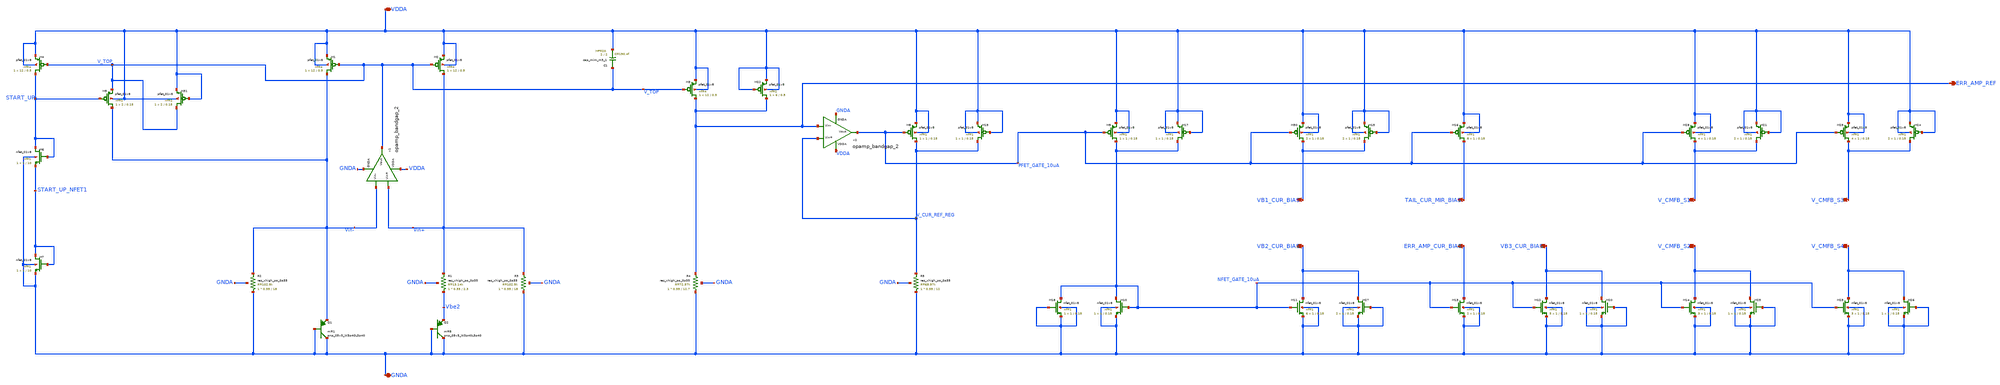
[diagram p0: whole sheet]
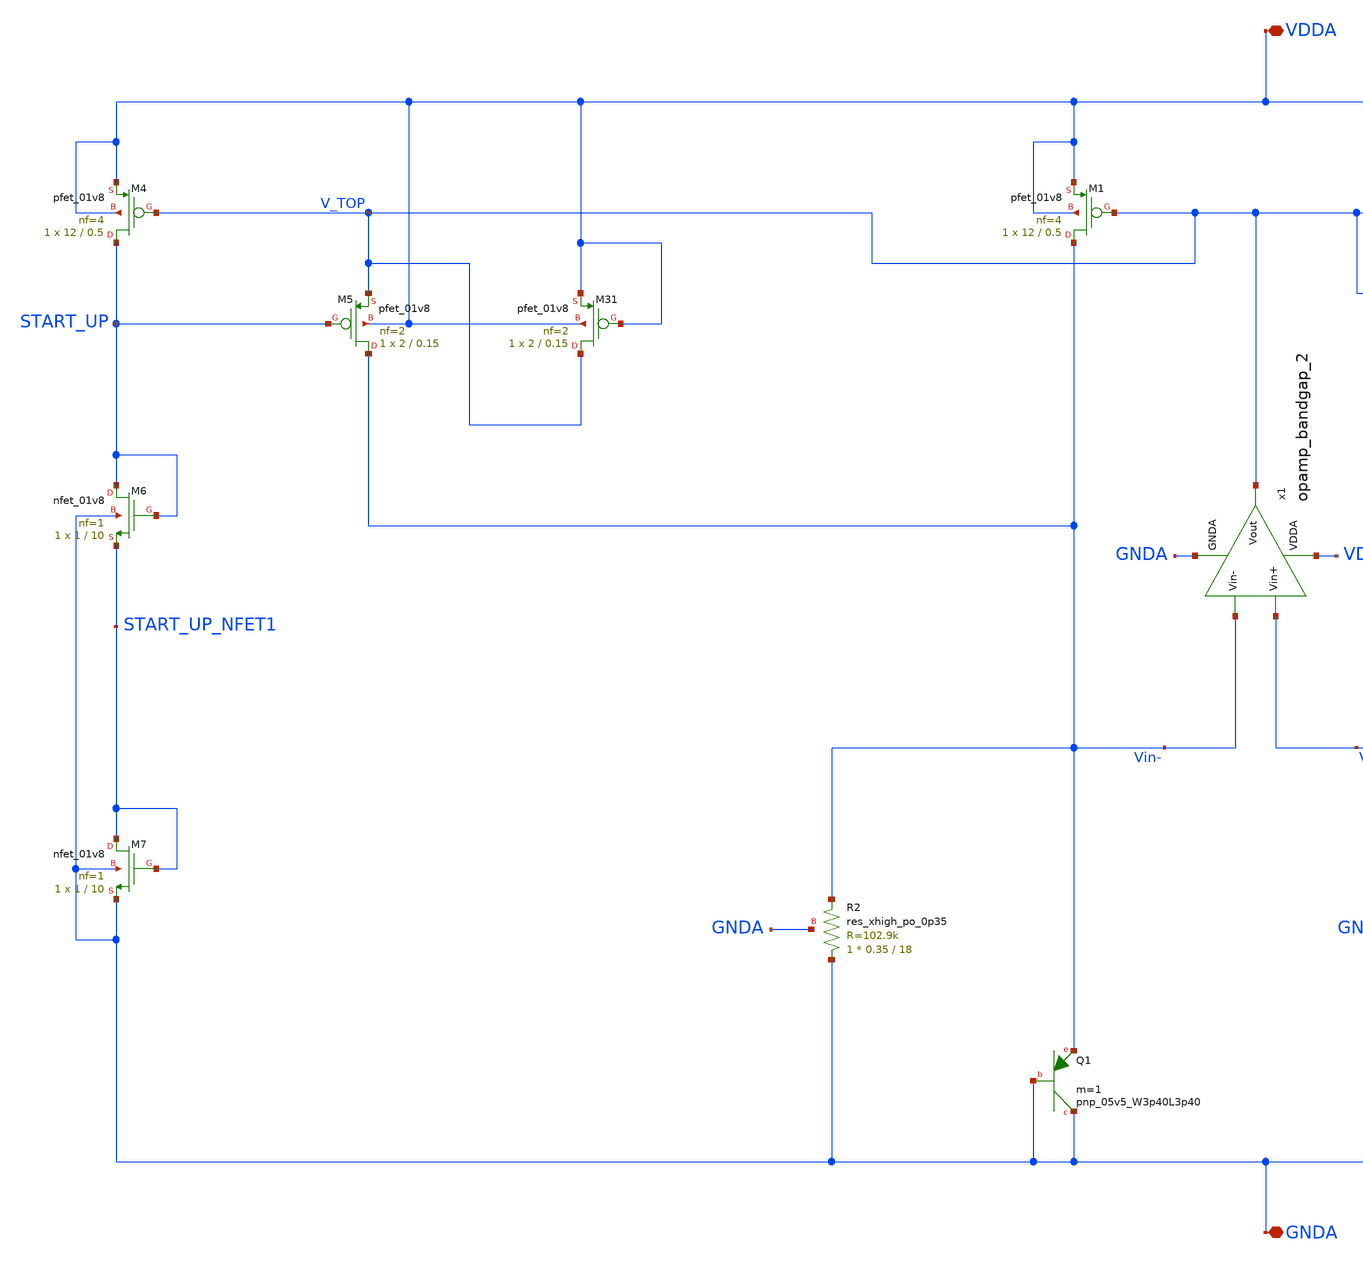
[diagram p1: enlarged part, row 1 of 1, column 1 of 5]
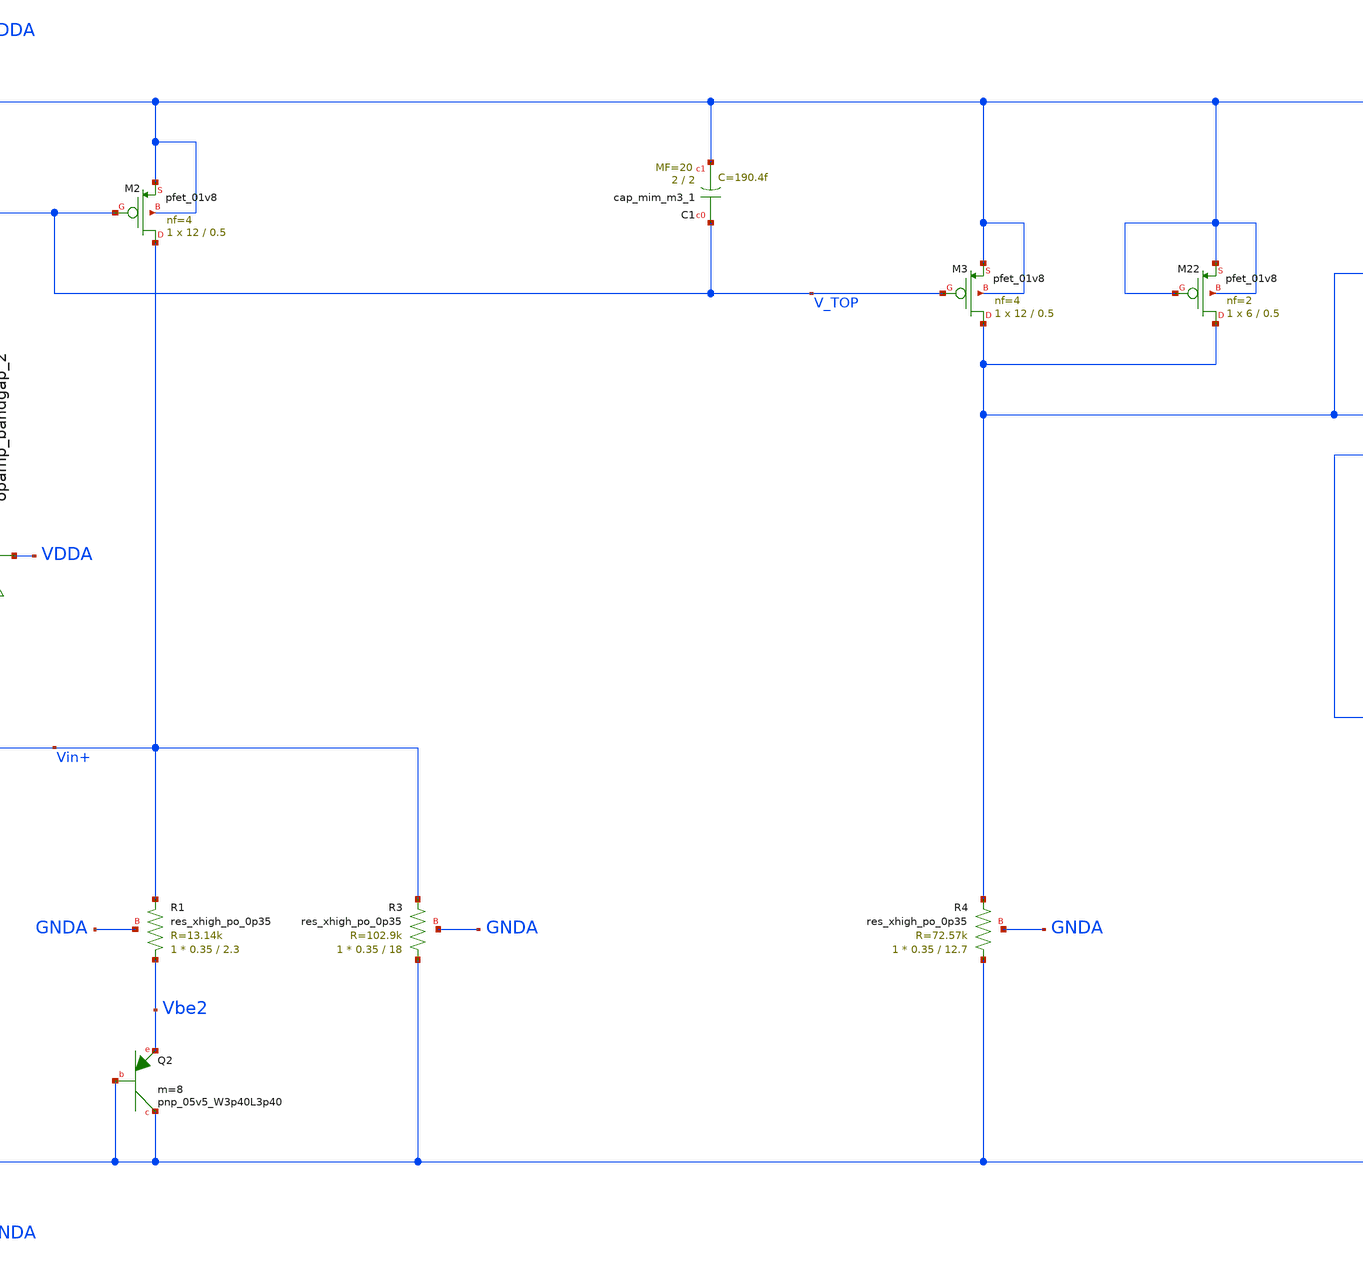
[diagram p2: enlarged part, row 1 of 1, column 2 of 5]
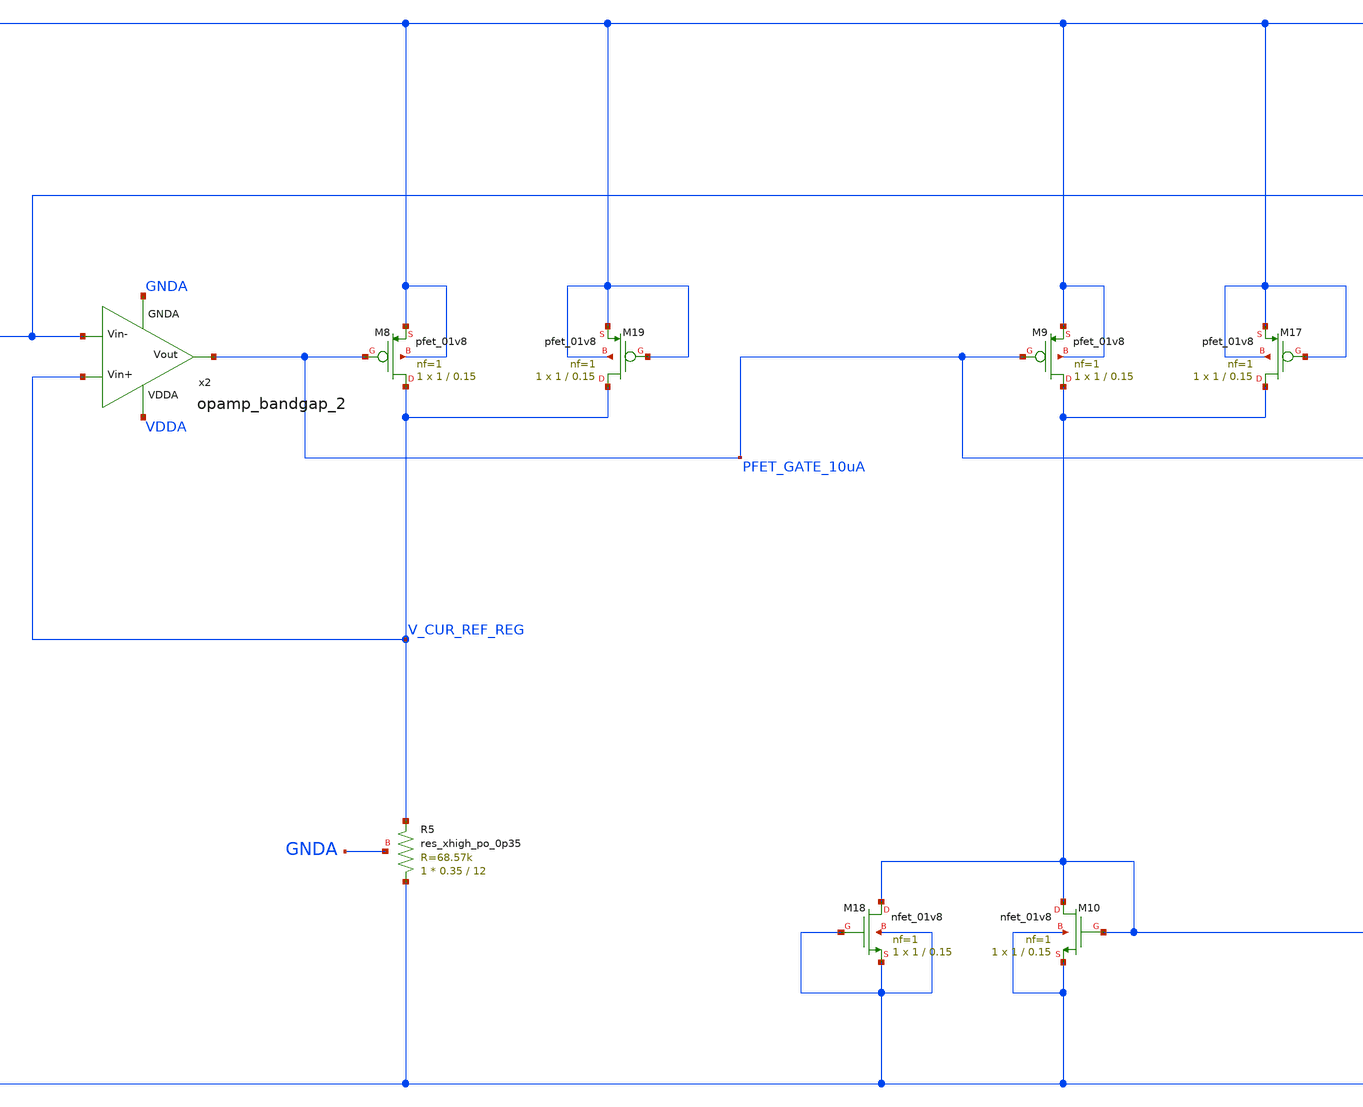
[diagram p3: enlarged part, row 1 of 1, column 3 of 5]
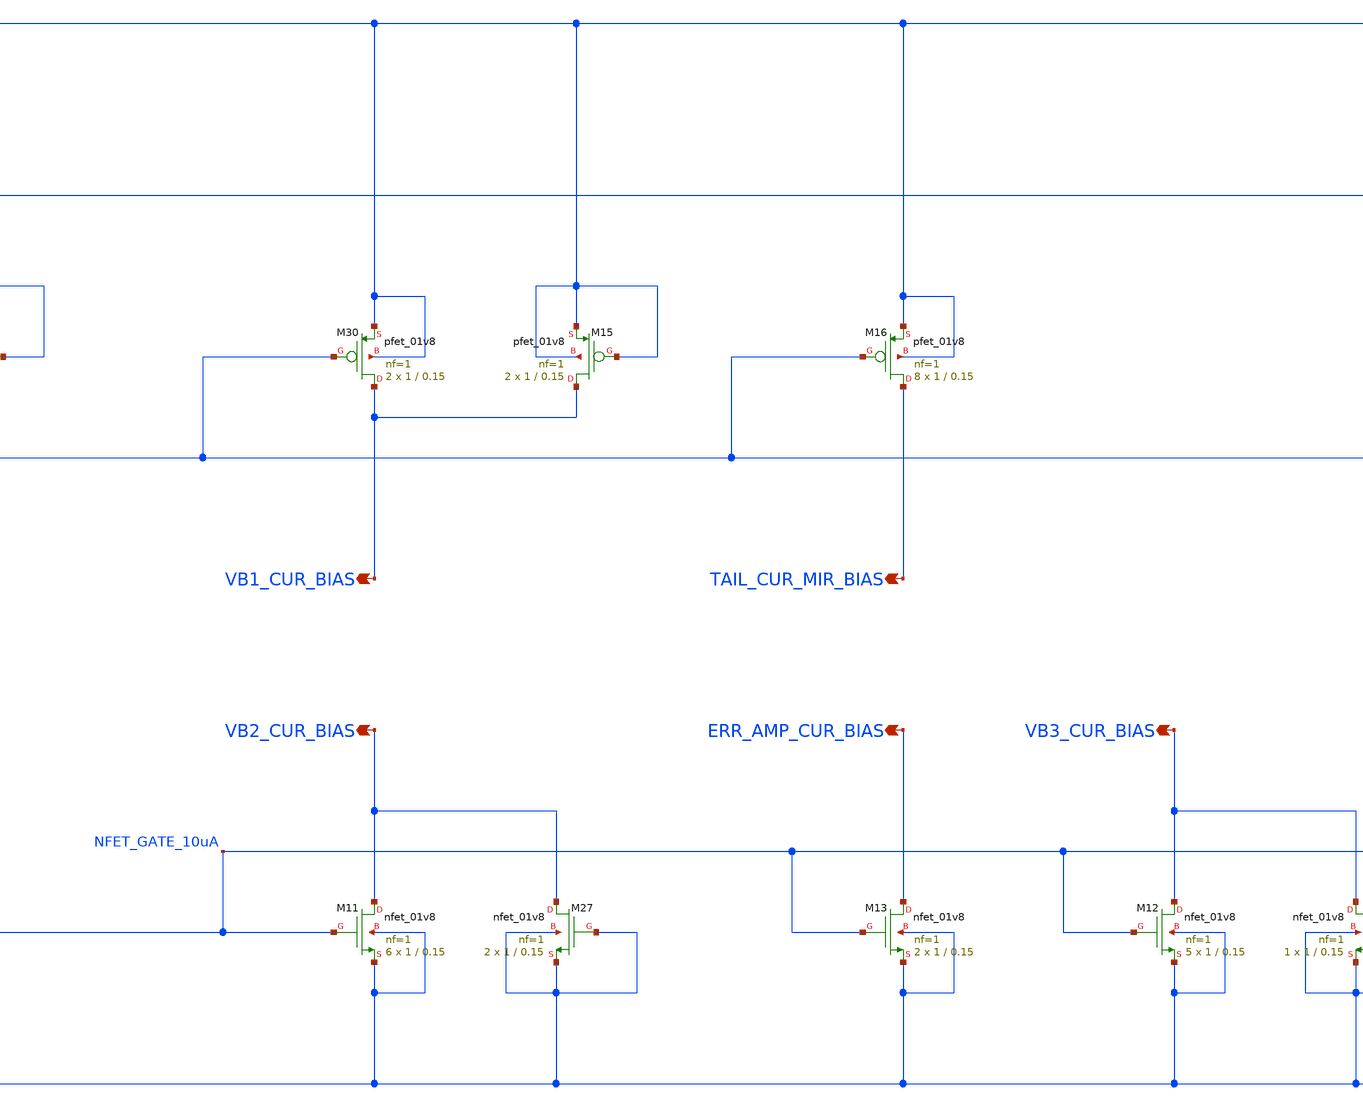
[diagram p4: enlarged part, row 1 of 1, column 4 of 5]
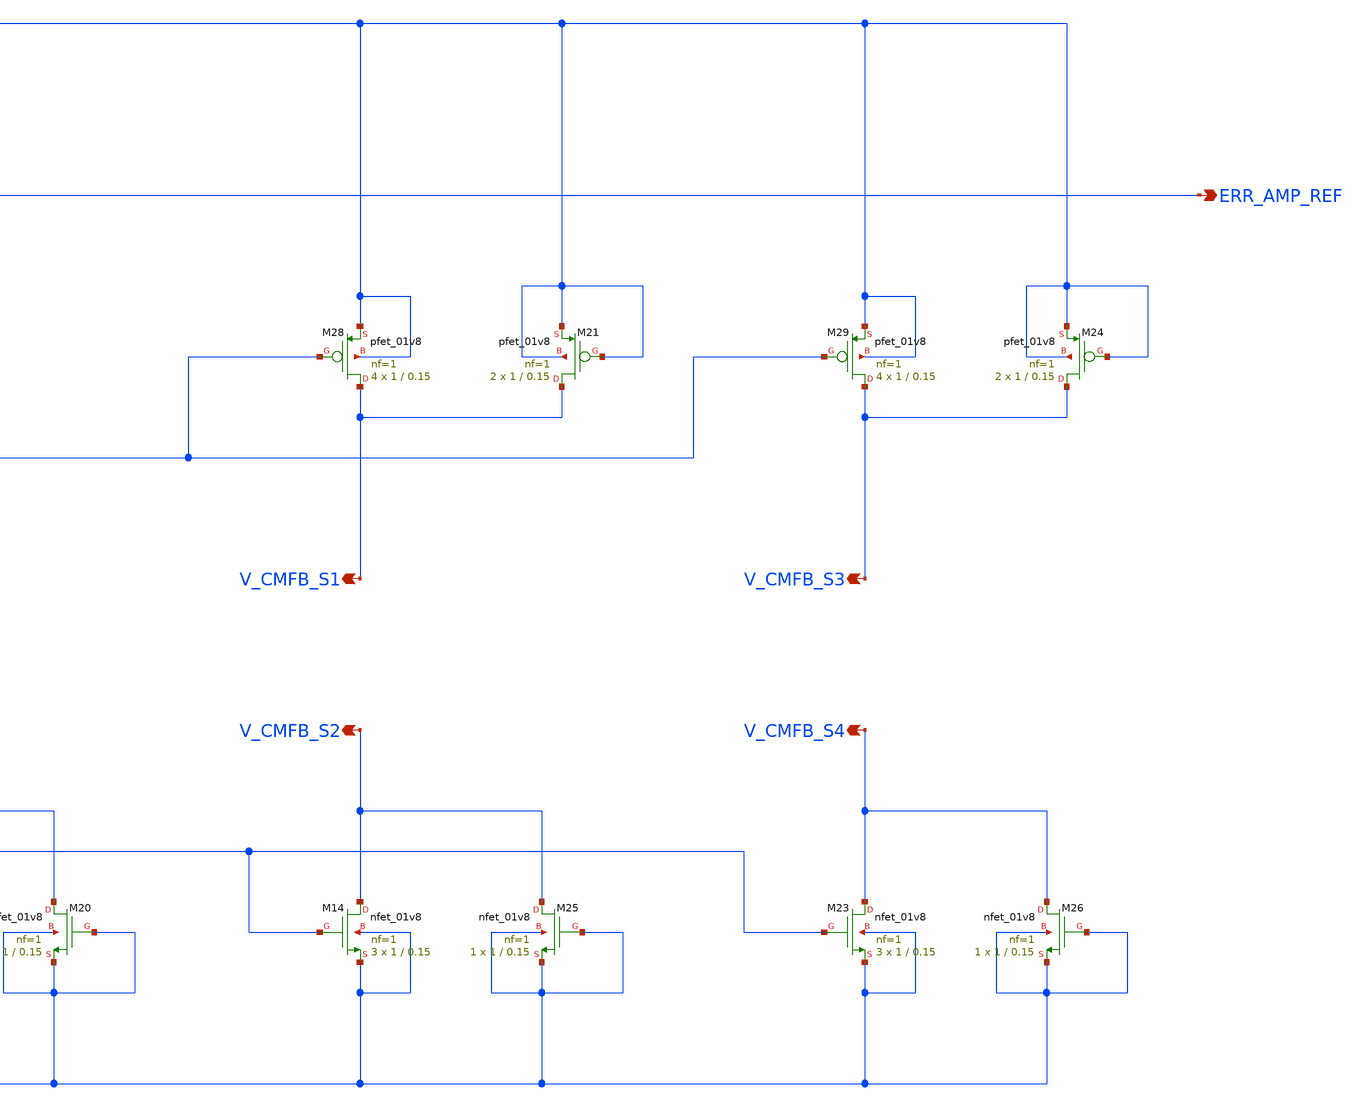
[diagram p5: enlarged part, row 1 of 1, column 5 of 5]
** sch_path: projects/opamp/xschem_ngspice/ref_volt_cur_gen_dummy.sch
**.subckt ref_volt_cur_gen_dummy VB1_CUR_BIAS GNDA ERR_AMP_REF VDDA VB2_CUR_BIAS VB3_CUR_BIAS
*+ ERR_AMP_CUR_BIAS V_CMFB_S2 TAIL_CUR_MIR_BIAS V_CMFB_S1 V_CMFB_S4 V_CMFB_S3
*.opin VB1_CUR_BIAS
*.iopin GNDA
*.opin ERR_AMP_REF
*.iopin VDDA
*.opin VB2_CUR_BIAS
*.opin VB3_CUR_BIAS
*.opin ERR_AMP_CUR_BIAS
*.opin V_CMFB_S2
*.opin TAIL_CUR_MIR_BIAS
*.opin V_CMFB_S1
*.opin V_CMFB_S4
*.opin V_CMFB_S3
XM3 ERR_AMP_REF V_TOP VDDA VDDA sky130_fd_pr__pfet_01v8 L=0.5 W=12 nf=4 ad='int((nf+1)/2) * W/nf * 0.29'
+ as='int((nf+2)/2) * W/nf * 0.29' pd='2*int((nf+1)/2) * (W/nf + 0.29)' ps='2*int((nf+2)/2) * (W/nf + 0.29)'
+ nrd='0.29 / W' nrs='0.29 / W' sa=0 sb=0 sd=0 mult=1 m=1
XR4 GNDA ERR_AMP_REF GNDA sky130_fd_pr__res_xhigh_po_0p35 L=12.7 mult=1 m=1
XR5 GNDA V_CUR_REF_REG GNDA sky130_fd_pr__res_xhigh_po_0p35 L=12 mult=1 m=1
XM8 V_CUR_REF_REG PFET_GATE_10uA VDDA VDDA sky130_fd_pr__pfet_01v8 L=0.15 W=1 nf=1 ad='int((nf+1)/2) * W/nf * 0.29'
+ as='int((nf+2)/2) * W/nf * 0.29' pd='2*int((nf+1)/2) * (W/nf + 0.29)' ps='2*int((nf+2)/2) * (W/nf + 0.29)'
+ nrd='0.29 / W' nrs='0.29 / W' sa=0 sb=0 sd=0 mult=1 m=1
XC1 V_TOP VDDA sky130_fd_pr__cap_mim_m3_1 W=2 L=2 MF=20 m=20
XQ1 GNDA GNDA Vin- sky130_fd_pr__pnp_05v5_W3p40L3p40 m=1
XQ2 GNDA GNDA Vbe2 sky130_fd_pr__pnp_05v5_W3p40L3p40 m=8
XM1 Vin- V_TOP VDDA VDDA sky130_fd_pr__pfet_01v8 L=0.5 W=12 nf=4 ad='int((nf+1)/2) * W/nf * 0.29' as='int((nf+2)/2) * W/nf * 0.29'
+ pd='2*int((nf+1)/2) * (W/nf + 0.29)' ps='2*int((nf+2)/2) * (W/nf + 0.29)' nrd='0.29 / W' nrs='0.29 / W'
+ sa=0 sb=0 sd=0 mult=1 m=1
XM2 Vin+ V_TOP VDDA VDDA sky130_fd_pr__pfet_01v8 L=0.5 W=12 nf=4 ad='int((nf+1)/2) * W/nf * 0.29' as='int((nf+2)/2) * W/nf * 0.29'
+ pd='2*int((nf+1)/2) * (W/nf + 0.29)' ps='2*int((nf+2)/2) * (W/nf + 0.29)' nrd='0.29 / W' nrs='0.29 / W'
+ sa=0 sb=0 sd=0 mult=1 m=1
XR1 Vbe2 Vin+ GNDA sky130_fd_pr__res_xhigh_po_0p35 L=2.3 mult=1 m=1
XR3 GNDA Vin+ GNDA sky130_fd_pr__res_xhigh_po_0p35 L=18 mult=1 m=1
XR2 GNDA Vin- GNDA sky130_fd_pr__res_xhigh_po_0p35 L=18 mult=1 m=1
XM6 START_UP START_UP START_UP_NFET1 GNDA sky130_fd_pr__nfet_01v8 L=10 W=1 nf=1 ad='int((nf+1)/2) * W/nf * 0.29'
+ as='int((nf+2)/2) * W/nf * 0.29' pd='2*int((nf+1)/2) * (W/nf + 0.29)' ps='2*int((nf+2)/2) * (W/nf + 0.29)'
+ nrd='0.29 / W' nrs='0.29 / W' sa=0 sb=0 sd=0 mult=1 m=1
XM4 START_UP V_TOP VDDA VDDA sky130_fd_pr__pfet_01v8 L=0.5 W=12 nf=4 ad='int((nf+1)/2) * W/nf * 0.29'
+ as='int((nf+2)/2) * W/nf * 0.29' pd='2*int((nf+1)/2) * (W/nf + 0.29)' ps='2*int((nf+2)/2) * (W/nf + 0.29)'
+ nrd='0.29 / W' nrs='0.29 / W' sa=0 sb=0 sd=0 mult=1 m=1
XM5 Vin- START_UP V_TOP VDDA sky130_fd_pr__pfet_01v8 L=0.15 W=2 nf=2 ad='int((nf+1)/2) * W/nf * 0.29'
+ as='int((nf+2)/2) * W/nf * 0.29' pd='2*int((nf+1)/2) * (W/nf + 0.29)' ps='2*int((nf+2)/2) * (W/nf + 0.29)'
+ nrd='0.29 / W' nrs='0.29 / W' sa=0 sb=0 sd=0 mult=1 m=1
XM7 START_UP_NFET1 START_UP_NFET1 GNDA GNDA sky130_fd_pr__nfet_01v8 L=10 W=1 nf=1 ad='int((nf+1)/2) * W/nf * 0.29'
+ as='int((nf+2)/2) * W/nf * 0.29' pd='2*int((nf+1)/2) * (W/nf + 0.29)' ps='2*int((nf+2)/2) * (W/nf + 0.29)'
+ nrd='0.29 / W' nrs='0.29 / W' sa=0 sb=0 sd=0 mult=1 m=1
x1 VDDA V_TOP Vin- Vin+ GNDA opamp_bandgap_2
x2 VDDA PFET_GATE_10uA ERR_AMP_REF V_CUR_REF_REG GNDA opamp_bandgap_2
XM9 NFET_GATE_10uA PFET_GATE_10uA VDDA VDDA sky130_fd_pr__pfet_01v8 L=0.15 W=1 nf=1 ad='int((nf+1)/2) * W/nf * 0.29'
+ as='int((nf+2)/2) * W/nf * 0.29' pd='2*int((nf+1)/2) * (W/nf + 0.29)' ps='2*int((nf+2)/2) * (W/nf + 0.29)'
+ nrd='0.29 / W' nrs='0.29 / W' sa=0 sb=0 sd=0 mult=1 m=1
XM10 NFET_GATE_10uA NFET_GATE_10uA GNDA GNDA sky130_fd_pr__nfet_01v8 L=0.15 W=1 nf=1 ad='int((nf+1)/2) * W/nf * 0.29'
+ as='int((nf+2)/2) * W/nf * 0.29' pd='2*int((nf+1)/2) * (W/nf + 0.29)' ps='2*int((nf+2)/2) * (W/nf + 0.29)'
+ nrd='0.29 / W' nrs='0.29 / W' sa=0 sb=0 sd=0 mult=1 m=1
XM11 VB2_CUR_BIAS NFET_GATE_10uA GNDA GNDA sky130_fd_pr__nfet_01v8 L=0.15 W=1 nf=1 ad='int((nf+1)/2) * W/nf * 0.29'
+ as='int((nf+2)/2) * W/nf * 0.29' pd='2*int((nf+1)/2) * (W/nf + 0.29)' ps='2*int((nf+2)/2) * (W/nf + 0.29)'
+ nrd='0.29 / W' nrs='0.29 / W' sa=0 sb=0 sd=0 mult=6 m=6
XM12 VB3_CUR_BIAS NFET_GATE_10uA GNDA GNDA sky130_fd_pr__nfet_01v8 L=0.15 W=1 nf=1 ad='int((nf+1)/2) * W/nf * 0.29'
+ as='int((nf+2)/2) * W/nf * 0.29' pd='2*int((nf+1)/2) * (W/nf + 0.29)' ps='2*int((nf+2)/2) * (W/nf + 0.29)'
+ nrd='0.29 / W' nrs='0.29 / W' sa=0 sb=0 sd=0 mult=5 m=5
XM30 VB1_CUR_BIAS PFET_GATE_10uA VDDA VDDA sky130_fd_pr__pfet_01v8 L=0.15 W=1 nf=1 ad='int((nf+1)/2) * W/nf * 0.29'
+ as='int((nf+2)/2) * W/nf * 0.29' pd='2*int((nf+1)/2) * (W/nf + 0.29)' ps='2*int((nf+2)/2) * (W/nf + 0.29)'
+ nrd='0.29 / W' nrs='0.29 / W' sa=0 sb=0 sd=0 mult=2 m=2
XM13 ERR_AMP_CUR_BIAS NFET_GATE_10uA GNDA GNDA sky130_fd_pr__nfet_01v8 L=0.15 W=1 nf=1 ad='int((nf+1)/2) * W/nf * 0.29'
+ as='int((nf+2)/2) * W/nf * 0.29' pd='2*int((nf+1)/2) * (W/nf + 0.29)' ps='2*int((nf+2)/2) * (W/nf + 0.29)'
+ nrd='0.29 / W' nrs='0.29 / W' sa=0 sb=0 sd=0 mult=2 m=2
XM14 V_CMFB_S2 NFET_GATE_10uA GNDA GNDA sky130_fd_pr__nfet_01v8 L=0.15 W=1 nf=1 ad='int((nf+1)/2) * W/nf * 0.29'
+ as='int((nf+2)/2) * W/nf * 0.29' pd='2*int((nf+1)/2) * (W/nf + 0.29)' ps='2*int((nf+2)/2) * (W/nf + 0.29)'
+ nrd='0.29 / W' nrs='0.29 / W' sa=0 sb=0 sd=0 mult=3 m=3
XM16 TAIL_CUR_MIR_BIAS PFET_GATE_10uA VDDA VDDA sky130_fd_pr__pfet_01v8 L=0.15 W=1 nf=1 ad='int((nf+1)/2) * W/nf * 0.29'
+ as='int((nf+2)/2) * W/nf * 0.29' pd='2*int((nf+1)/2) * (W/nf + 0.29)' ps='2*int((nf+2)/2) * (W/nf + 0.29)'
+ nrd='0.29 / W' nrs='0.29 / W' sa=0 sb=0 sd=0 mult=8 m=8
XM17 NFET_GATE_10uA VDDA VDDA VDDA sky130_fd_pr__pfet_01v8 L=0.15 W=1 nf=1 ad='int((nf+1)/2) * W/nf * 0.29'
+ as='int((nf+2)/2) * W/nf * 0.29' pd='2*int((nf+1)/2) * (W/nf + 0.29)' ps='2*int((nf+2)/2) * (W/nf + 0.29)'
+ nrd='0.29 / W' nrs='0.29 / W' sa=0 sb=0 sd=0 mult=1 m=1
XM18 NFET_GATE_10uA GNDA GNDA GNDA sky130_fd_pr__nfet_01v8 L=0.15 W=1 nf=1 ad='int((nf+1)/2) * W/nf * 0.29'
+ as='int((nf+2)/2) * W/nf * 0.29' pd='2*int((nf+1)/2) * (W/nf + 0.29)' ps='2*int((nf+2)/2) * (W/nf + 0.29)'
+ nrd='0.29 / W' nrs='0.29 / W' sa=0 sb=0 sd=0 mult=1 m=1
XM19 V_CUR_REF_REG VDDA VDDA VDDA sky130_fd_pr__pfet_01v8 L=0.15 W=1 nf=1 ad='int((nf+1)/2) * W/nf * 0.29'
+ as='int((nf+2)/2) * W/nf * 0.29' pd='2*int((nf+1)/2) * (W/nf + 0.29)' ps='2*int((nf+2)/2) * (W/nf + 0.29)'
+ nrd='0.29 / W' nrs='0.29 / W' sa=0 sb=0 sd=0 mult=1 m=1
XM20 VB3_CUR_BIAS GNDA GNDA GNDA sky130_fd_pr__nfet_01v8 L=0.15 W=1 nf=1 ad='int((nf+1)/2) * W/nf * 0.29'
+ as='int((nf+2)/2) * W/nf * 0.29' pd='2*int((nf+1)/2) * (W/nf + 0.29)' ps='2*int((nf+2)/2) * (W/nf + 0.29)'
+ nrd='0.29 / W' nrs='0.29 / W' sa=0 sb=0 sd=0 mult=1 m=1
XM28 V_CMFB_S1 PFET_GATE_10uA VDDA VDDA sky130_fd_pr__pfet_01v8 L=0.15 W=1 nf=1 ad='int((nf+1)/2) * W/nf * 0.29'
+ as='int((nf+2)/2) * W/nf * 0.29' pd='2*int((nf+1)/2) * (W/nf + 0.29)' ps='2*int((nf+2)/2) * (W/nf + 0.29)'
+ nrd='0.29 / W' nrs='0.29 / W' sa=0 sb=0 sd=0 mult=4 m=4
XM22 ERR_AMP_REF VDDA VDDA VDDA sky130_fd_pr__pfet_01v8 L=0.5 W=6 nf=2 ad='int((nf+1)/2) * W/nf * 0.29'
+ as='int((nf+2)/2) * W/nf * 0.29' pd='2*int((nf+1)/2) * (W/nf + 0.29)' ps='2*int((nf+2)/2) * (W/nf + 0.29)'
+ nrd='0.29 / W' nrs='0.29 / W' sa=0 sb=0 sd=0 mult=1 m=1
XM23 V_CMFB_S4 NFET_GATE_10uA GNDA GNDA sky130_fd_pr__nfet_01v8 L=0.15 W=1 nf=1 ad='int((nf+1)/2) * W/nf * 0.29'
+ as='int((nf+2)/2) * W/nf * 0.29' pd='2*int((nf+1)/2) * (W/nf + 0.29)' ps='2*int((nf+2)/2) * (W/nf + 0.29)'
+ nrd='0.29 / W' nrs='0.29 / W' sa=0 sb=0 sd=0 mult=3 m=3
XM29 V_CMFB_S3 PFET_GATE_10uA VDDA VDDA sky130_fd_pr__pfet_01v8 L=0.15 W=1 nf=1 ad='int((nf+1)/2) * W/nf * 0.29'
+ as='int((nf+2)/2) * W/nf * 0.29' pd='2*int((nf+1)/2) * (W/nf + 0.29)' ps='2*int((nf+2)/2) * (W/nf + 0.29)'
+ nrd='0.29 / W' nrs='0.29 / W' sa=0 sb=0 sd=0 mult=4 m=4
XM25 V_CMFB_S2 GNDA GNDA GNDA sky130_fd_pr__nfet_01v8 L=0.15 W=1 nf=1 ad='int((nf+1)/2) * W/nf * 0.29'
+ as='int((nf+2)/2) * W/nf * 0.29' pd='2*int((nf+1)/2) * (W/nf + 0.29)' ps='2*int((nf+2)/2) * (W/nf + 0.29)'
+ nrd='0.29 / W' nrs='0.29 / W' sa=0 sb=0 sd=0 mult=1 m=1
XM26 V_CMFB_S4 GNDA GNDA GNDA sky130_fd_pr__nfet_01v8 L=0.15 W=1 nf=1 ad='int((nf+1)/2) * W/nf * 0.29'
+ as='int((nf+2)/2) * W/nf * 0.29' pd='2*int((nf+1)/2) * (W/nf + 0.29)' ps='2*int((nf+2)/2) * (W/nf + 0.29)'
+ nrd='0.29 / W' nrs='0.29 / W' sa=0 sb=0 sd=0 mult=1 m=1
XM27 VB2_CUR_BIAS GNDA GNDA GNDA sky130_fd_pr__nfet_01v8 L=0.15 W=1 nf=1 ad='int((nf+1)/2) * W/nf * 0.29'
+ as='int((nf+2)/2) * W/nf * 0.29' pd='2*int((nf+1)/2) * (W/nf + 0.29)' ps='2*int((nf+2)/2) * (W/nf + 0.29)'
+ nrd='0.29 / W' nrs='0.29 / W' sa=0 sb=0 sd=0 mult=2 m=2
XM21 V_CMFB_S1 VDDA VDDA VDDA sky130_fd_pr__pfet_01v8 L=0.15 W=1 nf=1 ad='int((nf+1)/2) * W/nf * 0.29'
+ as='int((nf+2)/2) * W/nf * 0.29' pd='2*int((nf+1)/2) * (W/nf + 0.29)' ps='2*int((nf+2)/2) * (W/nf + 0.29)'
+ nrd='0.29 / W' nrs='0.29 / W' sa=0 sb=0 sd=0 mult=2 m=2
XM24 V_CMFB_S3 VDDA VDDA VDDA sky130_fd_pr__pfet_01v8 L=0.15 W=1 nf=1 ad='int((nf+1)/2) * W/nf * 0.29'
+ as='int((nf+2)/2) * W/nf * 0.29' pd='2*int((nf+1)/2) * (W/nf + 0.29)' ps='2*int((nf+2)/2) * (W/nf + 0.29)'
+ nrd='0.29 / W' nrs='0.29 / W' sa=0 sb=0 sd=0 mult=2 m=2
XM15 VB1_CUR_BIAS VDDA VDDA VDDA sky130_fd_pr__pfet_01v8 L=0.15 W=1 nf=1 ad='int((nf+1)/2) * W/nf * 0.29'
+ as='int((nf+2)/2) * W/nf * 0.29' pd='2*int((nf+1)/2) * (W/nf + 0.29)' ps='2*int((nf+2)/2) * (W/nf + 0.29)'
+ nrd='0.29 / W' nrs='0.29 / W' sa=0 sb=0 sd=0 mult=2 m=2
XM31 V_TOP VDDA VDDA VDDA sky130_fd_pr__pfet_01v8 L=0.15 W=2 nf=2 ad='int((nf+1)/2) * W/nf * 0.29' as='int((nf+2)/2) * W/nf * 0.29'
+ pd='2*int((nf+1)/2) * (W/nf + 0.29)' ps='2*int((nf+2)/2) * (W/nf + 0.29)' nrd='0.29 / W' nrs='0.29 / W'
+ sa=0 sb=0 sd=0 mult=1 m=1
**.ends

* expanding   symbol:
*+  /foss/designs/my_design/projects/bandgapref/xschem_ngspice/new_files/opamp_bandgap_2.sym # of pins=5
** sym_path: projects/bandgapref/xschem_ngspice/new_files/opamp_bandgap_2.sym
** sch_path: projects/bandgapref/xschem_ngspice/new_files/opamp_bandgap_2.sch
.subckt opamp_bandgap_2 VDDA Vout Vin- Vin+ GNDA
*.ipin Vin+
*.opin Vout
*.ipin Vin-
*.ipin GNDA
*.ipin VDDA
XM1 V_p VDDA GNDA GNDA sky130_fd_pr__nfet_01v8 L=5 W=2.5 nf=1 ad='int((nf+1)/2) * W/nf * 0.29' as='int((nf+2)/2) * W/nf * 0.29'
+ pd='2*int((nf+1)/2) * (W/nf + 0.29)' ps='2*int((nf+2)/2) * (W/nf + 0.29)' nrd='0.29 / W' nrs='0.29 / W'
+ sa=0 sb=0 sd=0 mult=1 m=1
XM2 V_mirror Vin- V_p GNDA sky130_fd_pr__nfet_01v8 L=0.2 W=2.5 nf=1 ad='int((nf+1)/2) * W/nf * 0.29'
+ as='int((nf+2)/2) * W/nf * 0.29' pd='2*int((nf+1)/2) * (W/nf + 0.29)' ps='2*int((nf+2)/2) * (W/nf + 0.29)'
+ nrd='0.29 / W' nrs='0.29 / W' sa=0 sb=0 sd=0 mult=1 m=1
XM3 1st_Vout Vin+ V_p GNDA sky130_fd_pr__nfet_01v8 L=0.2 W=2.5 nf=1 ad='int((nf+1)/2) * W/nf * 0.29'
+ as='int((nf+2)/2) * W/nf * 0.29' pd='2*int((nf+1)/2) * (W/nf + 0.29)' ps='2*int((nf+2)/2) * (W/nf + 0.29)'
+ nrd='0.29 / W' nrs='0.29 / W' sa=0 sb=0 sd=0 mult=1 m=1
XM5 V_mirror V_mirror VDDA VDDA sky130_fd_pr__pfet_01v8 L=0.2 W=6 nf=2 ad='int((nf+1)/2) * W/nf * 0.29'
+ as='int((nf+2)/2) * W/nf * 0.29' pd='2*int((nf+1)/2) * (W/nf + 0.29)' ps='2*int((nf+2)/2) * (W/nf + 0.29)'
+ nrd='0.29 / W' nrs='0.29 / W' sa=0 sb=0 sd=0 mult=1 m=1
XM6 1st_Vout V_mirror VDDA VDDA sky130_fd_pr__pfet_01v8 L=0.2 W=6 nf=2 ad='int((nf+1)/2) * W/nf * 0.29'
+ as='int((nf+2)/2) * W/nf * 0.29' pd='2*int((nf+1)/2) * (W/nf + 0.29)' ps='2*int((nf+2)/2) * (W/nf + 0.29)'
+ nrd='0.29 / W' nrs='0.29 / W' sa=0 sb=0 sd=0 mult=1 m=1
XM4 Vout VDDA GNDA GNDA sky130_fd_pr__nfet_01v8 L=5 W=2.5 nf=1 ad='int((nf+1)/2) * W/nf * 0.29' as='int((nf+2)/2) * W/nf * 0.29'
+ pd='2*int((nf+1)/2) * (W/nf + 0.29)' ps='2*int((nf+2)/2) * (W/nf + 0.29)' nrd='0.29 / W' nrs='0.29 / W'
+ sa=0 sb=0 sd=0 mult=1 m=1
XM7 Vout 1st_Vout VDDA VDDA sky130_fd_pr__pfet_01v8 L=0.2 W=6 nf=2 ad='int((nf+1)/2) * W/nf * 0.29' as='int((nf+2)/2) * W/nf * 0.29'
+ pd='2*int((nf+1)/2) * (W/nf + 0.29)' ps='2*int((nf+2)/2) * (W/nf + 0.29)' nrd='0.29 / W' nrs='0.29 / W'
+ sa=0 sb=0 sd=0 mult=1 m=1
XC1 1st_Vout cap_res sky130_fd_pr__cap_mim_m3_1 W=2 L=2 MF=20 m=20
XM8 Vout VDDA VDDA VDDA sky130_fd_pr__pfet_01v8 L=0.2 W=1 nf=1 ad='int((nf+1)/2) * W/nf * 0.29' as='int((nf+2)/2) * W/nf * 0.29'
+ pd='2*int((nf+1)/2) * (W/nf + 0.29)' ps='2*int((nf+2)/2) * (W/nf + 0.29)' nrd='0.29 / W' nrs='0.29 / W'
+ sa=0 sb=0 sd=0 mult=2 m=2
XR2 Vout cap_res GNDA sky130_fd_pr__res_high_po_0p35 L=2.05 mult=1 m=1
.ends

.end
